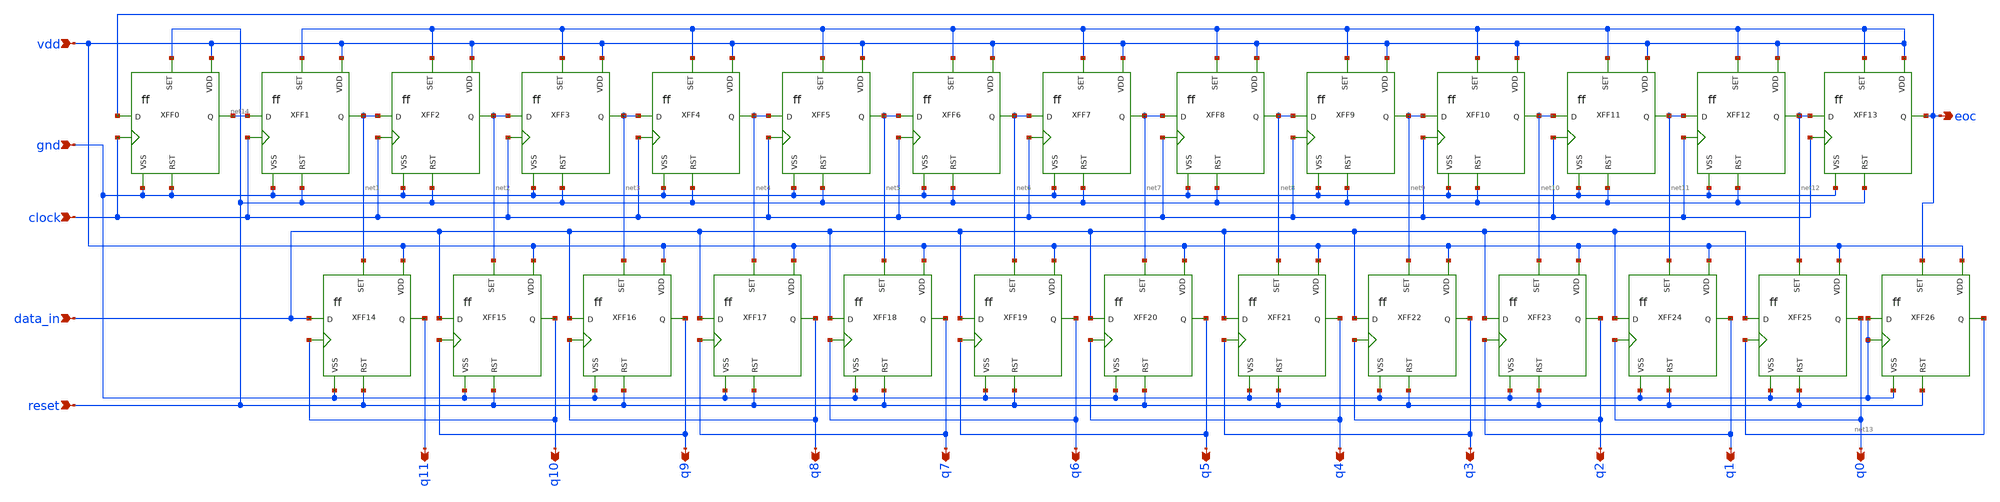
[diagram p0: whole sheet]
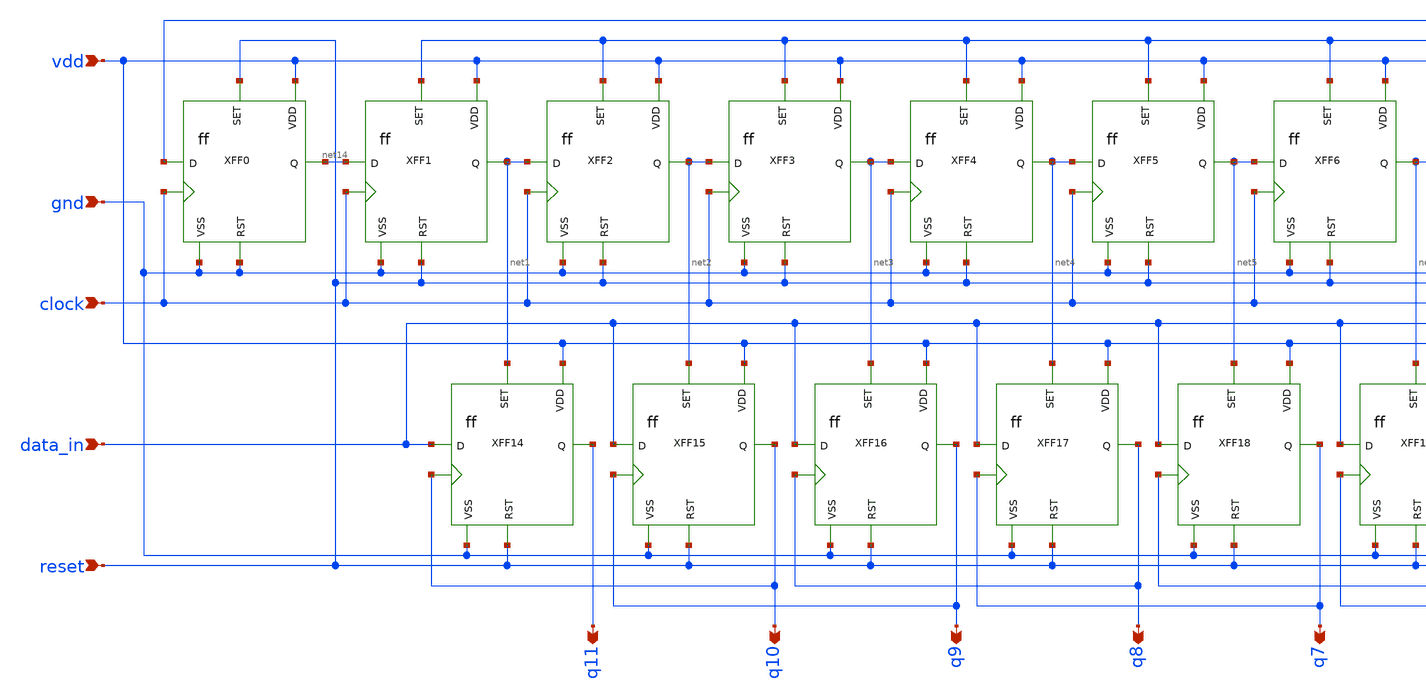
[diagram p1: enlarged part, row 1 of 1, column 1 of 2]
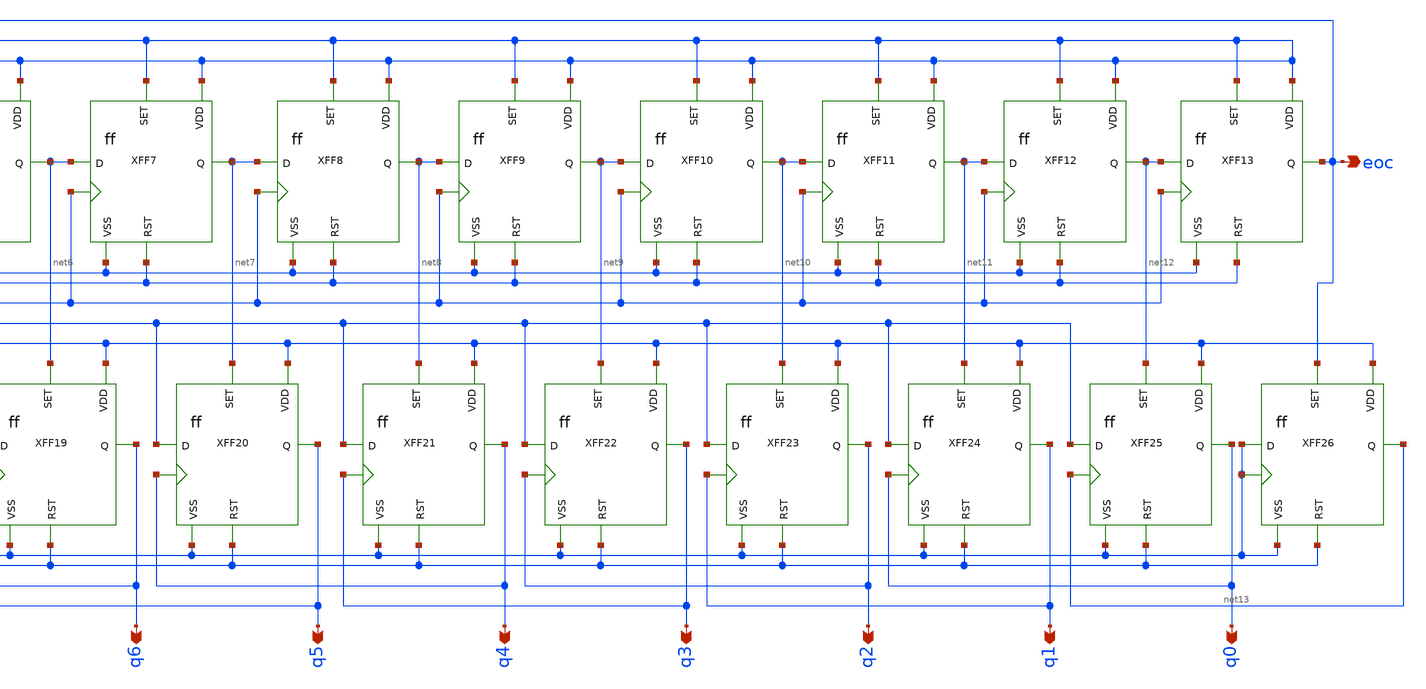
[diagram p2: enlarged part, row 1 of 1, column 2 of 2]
** sch_path: SAR_ADC/xschem/spice/sar_logic.sch
**.subckt sar_logic q11 eoc clock data_in reset gnd vdd q10 q9 q8 q7 q6 q5 q4 q3 q2 q1 q0
*.opin q11
*.opin eoc
*.ipin clock
*.ipin data_in
*.ipin reset
*.ipin gnd
*.ipin vdd
*.opin q10
*.opin q9
*.opin q8
*.opin q7
*.opin q6
*.opin q5
*.opin q4
*.opin q3
*.opin q2
*.opin q1
*.opin q0
XFF0 eoc clock reset gnd net14 gnd vdd ff
XFF1 net14 clock vdd reset net1 gnd vdd ff
XFF2 net1 clock vdd reset net2 gnd vdd ff
XFF14 data_in q10 net1 reset q11 gnd vdd ff
XFF3 net2 clock vdd reset net3 gnd vdd ff
XFF15 data_in q9 net2 reset q10 gnd vdd ff
XFF4 net3 clock vdd reset net4 gnd vdd ff
XFF16 data_in q8 net3 reset q9 gnd vdd ff
XFF17 data_in q7 net4 reset q8 gnd vdd ff
XFF5 net4 clock vdd reset net5 gnd vdd ff
XFF18 data_in q6 net5 reset q7 gnd vdd ff
XFF19 data_in q5 net6 reset q6 gnd vdd ff
XFF6 net5 clock vdd reset net6 gnd vdd ff
XFF7 net6 clock vdd reset net7 gnd vdd ff
XFF8 net7 clock vdd reset net8 gnd vdd ff
XFF9 net8 clock vdd reset net9 gnd vdd ff
XFF20 data_in q4 net7 reset q5 gnd vdd ff
XFF21 data_in q3 net8 reset q4 gnd vdd ff
XFF22 data_in q2 net9 reset q3 gnd vdd ff
XFF23 data_in q1 net10 reset q2 gnd vdd ff
XFF10 net9 clock vdd reset net10 gnd vdd ff
XFF11 net10 clock vdd reset net11 gnd vdd ff
XFF12 net11 clock vdd reset net12 gnd vdd ff
XFF24 data_in q0 net11 reset q1 gnd vdd ff
XFF13 net12 clock vdd reset eoc gnd vdd ff
XFF25 data_in net13 net12 reset q0 gnd vdd ff
XFF26 gnd gnd eoc reset net13 gnd vdd ff
**.ends

* expanding   symbol:  /foss/designs/sar_adc/xschem/spice/ff.sym # of pins=7
** sym_path: SAR_ADC/xschem/spice/ff.sym
** sch_path: SAR_ADC/xschem/spice/ff.sch
.subckt ff data_in clock set reset data_out gnd vdd
*.ipin data_in
*.ipin clock
*.ipin vdd
*.ipin gnd
*.opin data_out
*.ipin set
*.ipin reset
XFF1 net2 net3 net4 clock net1 vdd gnd gnd gnd gf180mcu_fd_sc_mcu7t5v0__dffrsnq_1
x1 vdd gnd net2 data_in inv cl=0.28u wp=0.44u wn=0.22u
x2 vdd gnd net4 reset inv cl=0.28u wp=0.44u wn=0.22u
x3 vdd gnd net3 set inv cl=0.28u wp=0.44u wn=0.22u
x4 vdd gnd data_out net1 inv cl=0.28u wp=0.44u wn=0.22u
.ends


* expanding   symbol:  /foss/designs/sar_adc/xschem/spice/inv.sym # of pins=4
** sym_path: SAR_ADC/xschem/spice/inv.sym
** sch_path: SAR_ADC/xschem/spice/inv.sch
.subckt inv vdd gnd vout vin  cl=0.28u wp=0.44u wn=0.22u
*.ipin gnd
*.ipin vdd
*.ipin vin
*.opin vout
XM1 gnd vin vout gnd nfet_03v3 L=0.28u W=4u nf=1 ad='int((nf+1)/2) * W/nf * 0.18u' as='int((nf+2)/2) * W/nf * 0.18u'
+ pd='2*int((nf+1)/2) * (W/nf + 0.18u)' ps='2*int((nf+2)/2) * (W/nf + 0.18u)' nrd='0.18u / W' nrs='0.18u / W'
+ sa=0 sb=0 sd=0 m=1
XM2 vdd vin vout vdd pfet_03v3 L=0.28u W=4u nf=1 ad='int((nf+1)/2) * W/nf * 0.18u' as='int((nf+2)/2) * W/nf * 0.18u'
+ pd='2*int((nf+1)/2) * (W/nf + 0.18u)' ps='2*int((nf+2)/2) * (W/nf + 0.18u)' nrd='0.18u / W' nrs='0.18u / W'
+ sa=0 sb=0 sd=0 m=1
.ends

.end
